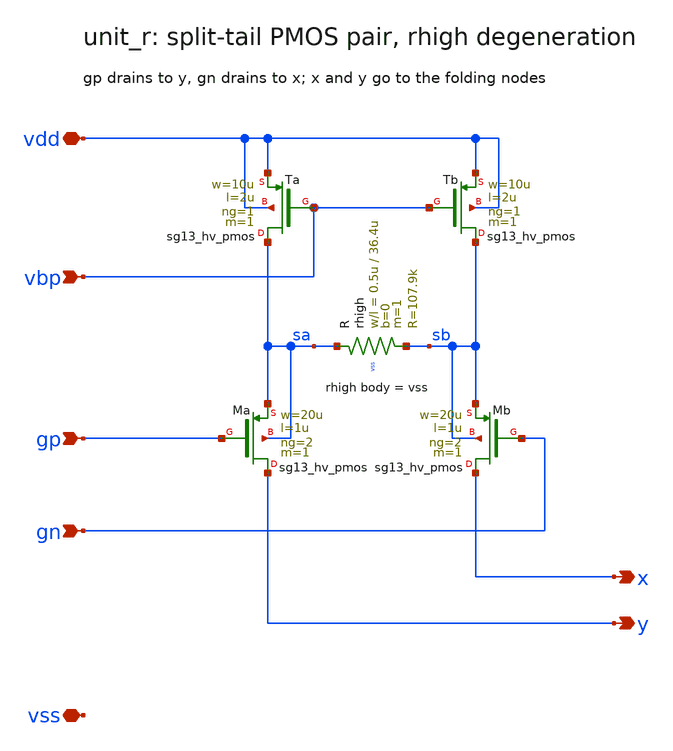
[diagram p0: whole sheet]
** sch_path: sudelbuecher/design_considerations/class_ab_pad_driver/improvements/xschem/unit_r.sch
**.subckt unit_r x y gp gn vdd vss vbp
*.opin x
*.opin y
*.ipin gp
*.ipin gn
*.iopin vdd
*.iopin vss
*.ipin vbp
XTa sa vbp vdd vdd sg13_hv_pmos w=10u l=2u ng=1 m=1 mm_ok=1
XTb sb vbp vdd vdd sg13_hv_pmos w=10u l=2u ng=1 m=1 mm_ok=1
XMa y gp sa sa sg13_hv_pmos w=20u l=1u ng=2 m=1 mm_ok=1
XMb x gn sb sb sg13_hv_pmos w=20u l=1u ng=2 m=1 mm_ok=1
XR sa sb vss rhigh w=0.5u l=36.4u m=1 b=0 mm_ok=1
**.ends
.end
